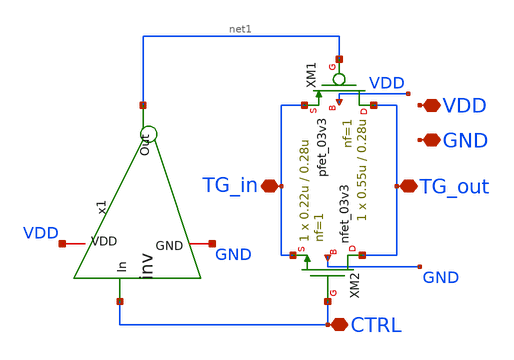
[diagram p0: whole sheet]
** sch_path: xschem/TG.sch
**.subckt TG TG_in TG_out VDD GND CTRL
*.iopin TG_in
*.iopin TG_out
*.iopin VDD
*.iopin GND
*.iopin CTRL
XM1 TG_out net1 TG_in VDD pfet_03v3 L=0.28u W=0.55u nf=1 ad='int((nf+1)/2) * W/nf * 0.18u' as='int((nf+2)/2) * W/nf * 0.18u'
+ pd='2*int((nf+1)/2) * (W/nf + 0.18u)' ps='2*int((nf+2)/2) * (W/nf + 0.18u)' nrd='0.18u / W' nrs='0.18u / W'
+ sa=0 sb=0 sd=0 m=1
XM2 TG_out CTRL TG_in GND nfet_03v3 L=0.28u W=0.22u nf=1 ad='int((nf+1)/2) * W/nf * 0.18u' as='int((nf+2)/2) * W/nf * 0.18u'
+ pd='2*int((nf+1)/2) * (W/nf + 0.18u)' ps='2*int((nf+2)/2) * (W/nf + 0.18u)' nrd='0.18u / W' nrs='0.18u / W'
+ sa=0 sb=0 sd=0 m=1
x1 VDD CTRL net1 GND inv
**.ends

* expanding   symbol:  inv.sym # of pins=4
** sym_path: xschem/inv.sym
** sch_path: xschem/inv.sch
.subckt inv VDD In Out GND
*.iopin VDD
*.iopin GND
*.ipin In
*.opin Out
XM3 Out In GND GND nfet_03v3 L=0.28u W=0.22u nf=1 ad='int((nf+1)/2) * W/nf * 0.18u' as='int((nf+2)/2) * W/nf * 0.18u'
+ pd='2*int((nf+1)/2) * (W/nf + 0.18u)' ps='2*int((nf+2)/2) * (W/nf + 0.18u)' nrd='0.18u / W' nrs='0.18u / W'
+ sa=0 sb=0 sd=0 m=1
XM2 Out In VDD VDD pfet_03v3 L=0.28u W=0.55u nf=1 ad='int((nf+1)/2) * W/nf * 0.18u' as='int((nf+2)/2) * W/nf * 0.18u'
+ pd='2*int((nf+1)/2) * (W/nf + 0.18u)' ps='2*int((nf+2)/2) * (W/nf + 0.18u)' nrd='0.18u / W' nrs='0.18u / W'
+ sa=0 sb=0 sd=0 m=1
.ends

.end
